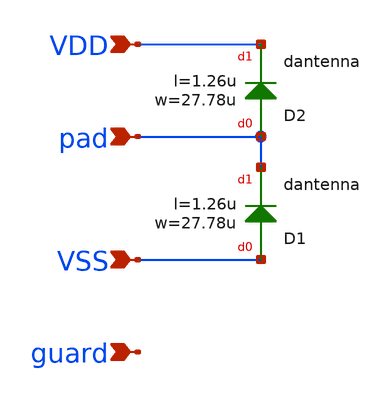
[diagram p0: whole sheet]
** sch_path: trident_test_structures/design_data/xschem/DCP_DCN_diodes.sch
**.subckt DCP_DCN_diodes VDD VSS pad guard
*.ipin VDD
*.ipin VSS
*.ipin pad
*.ipin guard
XD1 VSS pad dantenna l=1.26u w=27.78u
XD2 pad VDD dantenna l=1.26u w=27.78u
**.ends
.end
